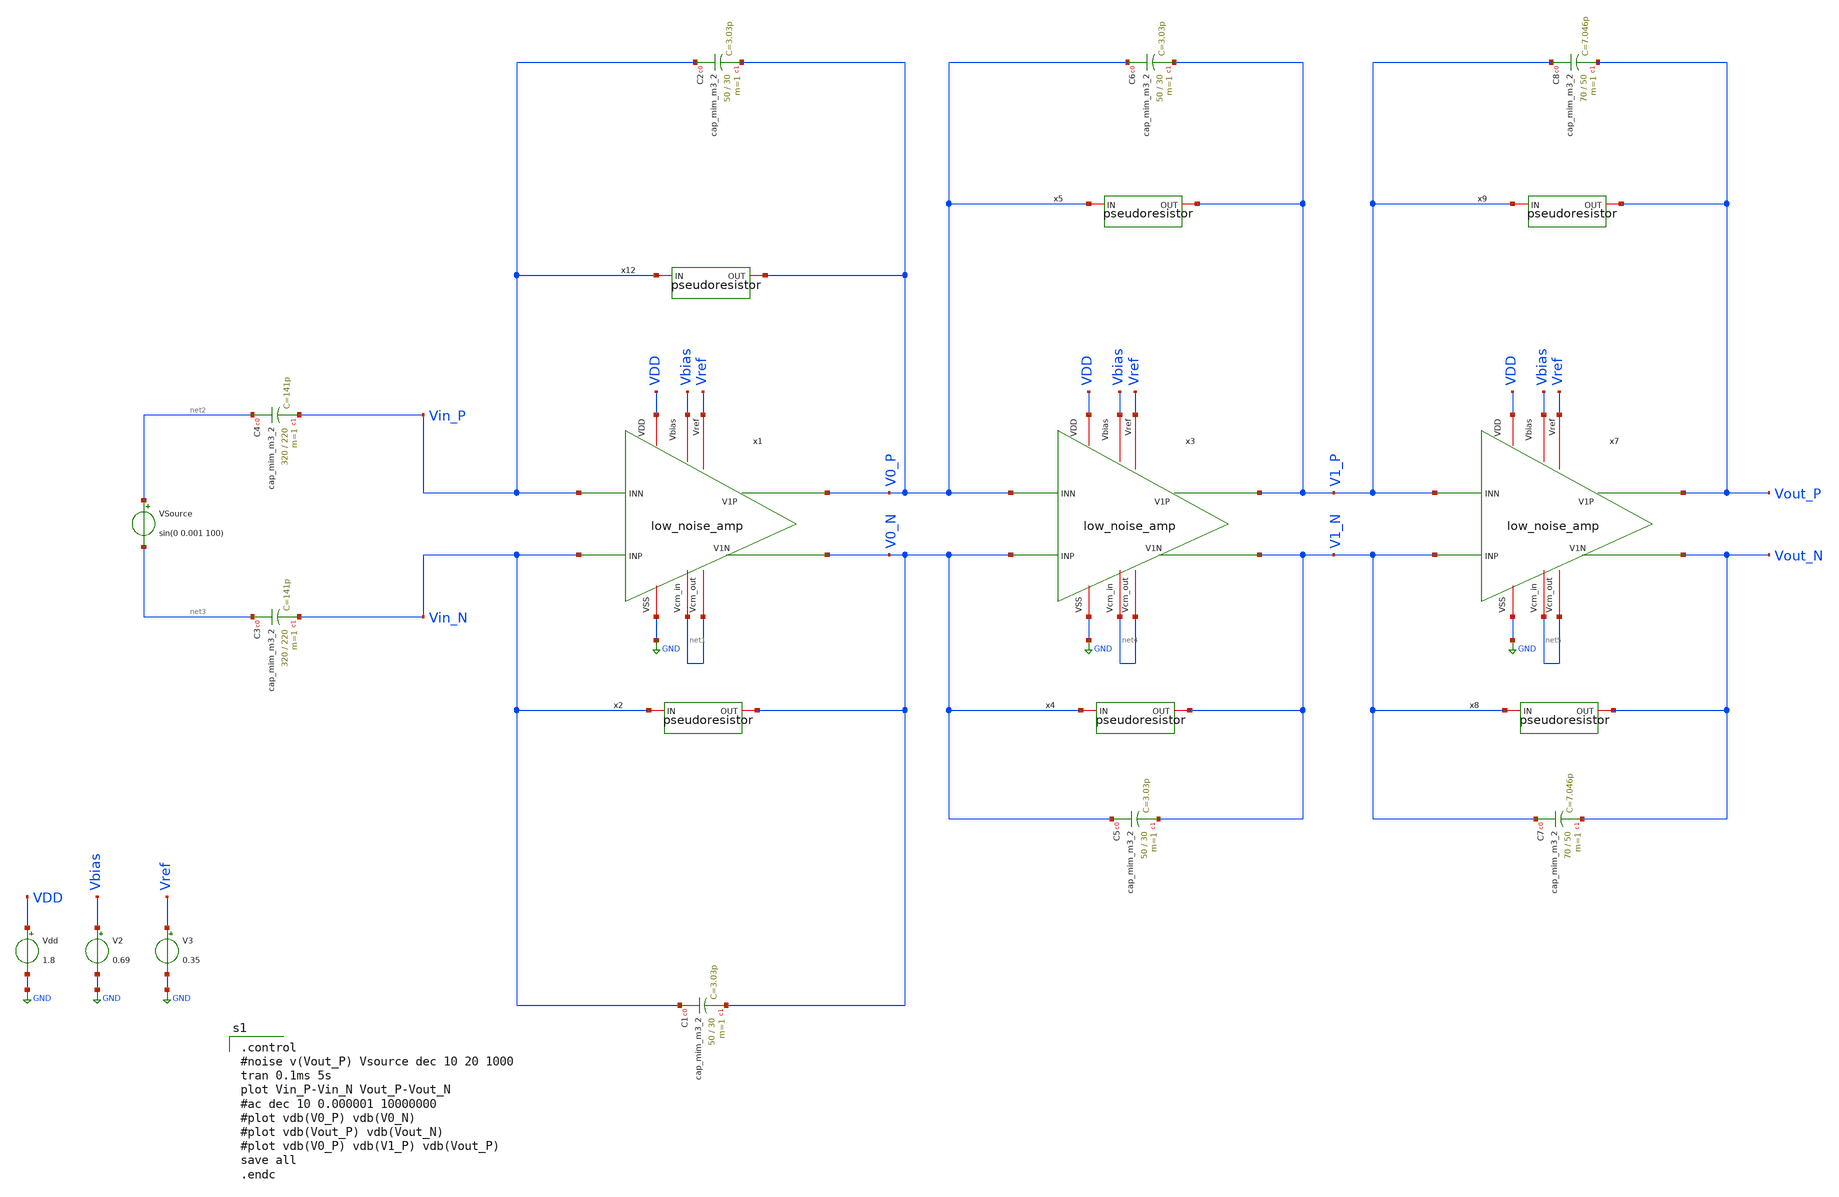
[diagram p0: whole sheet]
** sch_path: opamp_lna/low_noise_amp_tb.sch
**.subckt low_noise_amp_tb
x1 VDD net1 Vin_P Vin_N V0_P V0_N GND net1 Vbias Vref low_noise_amp
Vdd VDD GND 1.8
V2 Vbias GND 0.69
V3 Vref GND 0.35
VSource net2 net3 sin(0 0.001 100)
x2 Vin_N V0_N pseudoresistor
XC1 Vin_N V0_N sky130_fd_pr__cap_mim_m3_2 W=50 L=30 MF=1 m=1
XC2 Vin_P V0_P sky130_fd_pr__cap_mim_m3_2 W=50 L=30 MF=1 m=1
XC3 net3 Vin_N sky130_fd_pr__cap_mim_m3_2 W=320 L=220 MF=1 m=1
XC4 net2 Vin_P sky130_fd_pr__cap_mim_m3_2 W=320 L=220 MF=1 m=1
x3 VDD net4 V0_P V0_N V1_P V1_N GND net4 Vbias Vref low_noise_amp
x4 V0_N V1_N pseudoresistor
XC5 V0_N V1_N sky130_fd_pr__cap_mim_m3_2 W=50 L=30 MF=1 m=1
XC6 V0_P V1_P sky130_fd_pr__cap_mim_m3_2 W=50 L=30 MF=1 m=1
x5 V0_P V1_P pseudoresistor
x7 VDD net5 V1_P V1_N Vout_P Vout_N GND net5 Vbias Vref low_noise_amp
x8 V1_N Vout_N pseudoresistor
XC7 V1_N Vout_N sky130_fd_pr__cap_mim_m3_2 W=70 L=50 MF=1 m=1
XC8 V1_P Vout_P sky130_fd_pr__cap_mim_m3_2 W=70 L=50 MF=1 m=1
x9 V1_P Vout_P pseudoresistor
x12 Vin_P V0_P pseudoresistor
**** begin user architecture code

** opencircuitdesign pdks install
.lib $::SKYWATER_MODELS/sky130.lib.spice tt



.control
#noise v(Vout_P) Vsource dec 10 20 1000
tran 0.1ms 5s
plot Vin_P-Vin_N Vout_P-Vout_N
#ac dec 10 0.000001 10000000
#plot vdb(V0_P) vdb(V0_N)
#plot vdb(Vout_P) vdb(Vout_N)
#plot vdb(V0_P) vdb(V1_P) vdb(Vout_P)
save all
.endc

**** end user architecture code
**.ends

* expanding   symbol:  low_noise_amp.sym # of pins=10
** sym_path: opamp_lna/low_noise_amp.sym
** sch_path: opamp_lna/low_noise_amp.sch
.subckt low_noise_amp VDD Vcm_in INN INP V1P V1N VSS Vcm_out Vbias Vref
*.iopin VDD
*.iopin VSS
*.iopin Vbias
*.ipin INP
*.ipin INN
*.iopin Vref
*.iopin Vcm_in
*.iopin Vcm_out
*.opin V1N
*.opin V1P
XM3 CMFB Vref A0 VDD sky130_fd_pr__pfet_01v8 L=0.8 W=12 nf=1 ad='int((nf+1)/2) * W/nf * 0.29' as='int((nf+2)/2) * W/nf * 0.29'
+ pd='2*int((nf+1)/2) * (W/nf + 0.29)' ps='2*int((nf+2)/2) * (W/nf + 0.29)' nrd='0.29 / W' nrs='0.29 / W'
+ sa=0 sb=0 sd=0 mult=1 m=1
XM11 A0 Vbias VDD VDD sky130_fd_pr__pfet_01v8 L=0.8 W=4 nf=1 ad='int((nf+1)/2) * W/nf * 0.29' as='int((nf+2)/2) * W/nf * 0.29'
+ pd='2*int((nf+1)/2) * (W/nf + 0.29)' ps='2*int((nf+2)/2) * (W/nf + 0.29)' nrd='0.29 / W' nrs='0.29 / W'
+ sa=0 sb=0 sd=0 mult=1 m=1
XM7 V1N INP B0 VDD sky130_fd_pr__pfet_01v8 L=2 W=18 nf=1 ad='int((nf+1)/2) * W/nf * 0.29' as='int((nf+2)/2) * W/nf * 0.29'
+ pd='2*int((nf+1)/2) * (W/nf + 0.29)' ps='2*int((nf+2)/2) * (W/nf + 0.29)' nrd='0.29 / W' nrs='0.29 / W'
+ sa=0 sb=0 sd=0 mult=1 m=1
XM8 V1P INN B0 VDD sky130_fd_pr__pfet_01v8 L=2 W=18 nf=1 ad='int((nf+1)/2) * W/nf * 0.29' as='int((nf+2)/2) * W/nf * 0.29'
+ pd='2*int((nf+1)/2) * (W/nf + 0.29)' ps='2*int((nf+2)/2) * (W/nf + 0.29)' nrd='0.29 / W' nrs='0.29 / W'
+ sa=0 sb=0 sd=0 mult=1 m=1
XM9 V1N INP B1 VSS sky130_fd_pr__nfet_01v8 L=1 W=12 nf=1 ad='int((nf+1)/2) * W/nf * 0.29' as='int((nf+2)/2) * W/nf * 0.29'
+ pd='2*int((nf+1)/2) * (W/nf + 0.29)' ps='2*int((nf+2)/2) * (W/nf + 0.29)' nrd='0.29 / W' nrs='0.29 / W'
+ sa=0 sb=0 sd=0 mult=1 m=1
XM12 B0 Vbias VDD VDD sky130_fd_pr__pfet_01v8 L=0.8 W=4 nf=1 ad='int((nf+1)/2) * W/nf * 0.29' as='int((nf+2)/2) * W/nf * 0.29'
+ pd='2*int((nf+1)/2) * (W/nf + 0.29)' ps='2*int((nf+2)/2) * (W/nf + 0.29)' nrd='0.29 / W' nrs='0.29 / W'
+ sa=0 sb=0 sd=0 mult=1 m=1
XM13 B1 CMFB VSS VSS sky130_fd_pr__nfet_01v8 L=0.8 W=2 nf=1 ad='int((nf+1)/2) * W/nf * 0.29' as='int((nf+2)/2) * W/nf * 0.29'
+ pd='2*int((nf+1)/2) * (W/nf + 0.29)' ps='2*int((nf+2)/2) * (W/nf + 0.29)' nrd='0.29 / W' nrs='0.29 / W'
+ sa=0 sb=0 sd=0 mult=1 m=1
XM15 Vcm_out Vcm_out net1 Vcm_out sky130_fd_pr__pfet_01v8 L=0.6 W=1 nf=1 ad='int((nf+1)/2) * W/nf * 0.29'
+ as='int((nf+2)/2) * W/nf * 0.29' pd='2*int((nf+1)/2) * (W/nf + 0.29)' ps='2*int((nf+2)/2) * (W/nf + 0.29)'
+ nrd='0.29 / W' nrs='0.29 / W' sa=0 sb=0 sd=0 mult=5 m=5
XM16 net1 V1P V1P V1P sky130_fd_pr__pfet_01v8 L=0.6 W=1 nf=1 ad='int((nf+1)/2) * W/nf * 0.29' as='int((nf+2)/2) * W/nf * 0.29'
+ pd='2*int((nf+1)/2) * (W/nf + 0.29)' ps='2*int((nf+2)/2) * (W/nf + 0.29)' nrd='0.29 / W' nrs='0.29 / W'
+ sa=0 sb=0 sd=0 mult=5 m=5
XM17 Vcm_out Vcm_out net2 Vcm_out sky130_fd_pr__pfet_01v8 L=0.6 W=1 nf=1 ad='int((nf+1)/2) * W/nf * 0.29'
+ as='int((nf+2)/2) * W/nf * 0.29' pd='2*int((nf+1)/2) * (W/nf + 0.29)' ps='2*int((nf+2)/2) * (W/nf + 0.29)'
+ nrd='0.29 / W' nrs='0.29 / W' sa=0 sb=0 sd=0 mult=5 m=5
XM18 net2 V1N V1N V1N sky130_fd_pr__pfet_01v8 L=0.6 W=1 nf=1 ad='int((nf+1)/2) * W/nf * 0.29' as='int((nf+2)/2) * W/nf * 0.29'
+ pd='2*int((nf+1)/2) * (W/nf + 0.29)' ps='2*int((nf+2)/2) * (W/nf + 0.29)' nrd='0.29 / W' nrs='0.29 / W'
+ sa=0 sb=0 sd=0 mult=5 m=5
XC1 Vcm_out VSS sky130_fd_pr__cap_mim_m3_1 W=1 L=1 MF=1 m=1
XM1 V1P INN B1 VSS sky130_fd_pr__nfet_01v8 L=1 W=12 nf=1 ad='int((nf+1)/2) * W/nf * 0.29' as='int((nf+2)/2) * W/nf * 0.29'
+ pd='2*int((nf+1)/2) * (W/nf + 0.29)' ps='2*int((nf+2)/2) * (W/nf + 0.29)' nrd='0.29 / W' nrs='0.29 / W'
+ sa=0 sb=0 sd=0 mult=1 m=1
XM2 A1 A1 VSS VSS sky130_fd_pr__nfet_01v8 L=0.8 W=6 nf=1 ad='int((nf+1)/2) * W/nf * 0.29' as='int((nf+2)/2) * W/nf * 0.29'
+ pd='2*int((nf+1)/2) * (W/nf + 0.29)' ps='2*int((nf+2)/2) * (W/nf + 0.29)' nrd='0.29 / W' nrs='0.29 / W'
+ sa=0 sb=0 sd=0 mult=1 m=1
XM5 CMFB A1 VSS VSS sky130_fd_pr__nfet_01v8 L=0.8 W=6 nf=1 ad='int((nf+1)/2) * W/nf * 0.29' as='int((nf+2)/2) * W/nf * 0.29'
+ pd='2*int((nf+1)/2) * (W/nf + 0.29)' ps='2*int((nf+2)/2) * (W/nf + 0.29)' nrd='0.29 / W' nrs='0.29 / W'
+ sa=0 sb=0 sd=0 mult=1 m=1
XM6 A1 Vcm_in A0 VDD sky130_fd_pr__pfet_01v8 L=0.8 W=12 nf=1 ad='int((nf+1)/2) * W/nf * 0.29' as='int((nf+2)/2) * W/nf * 0.29'
+ pd='2*int((nf+1)/2) * (W/nf + 0.29)' ps='2*int((nf+2)/2) * (W/nf + 0.29)' nrd='0.29 / W' nrs='0.29 / W'
+ sa=0 sb=0 sd=0 mult=1 m=1
.ends


* expanding   symbol:  /home/lcg3895/CE393/pseudoresistor.sym # of pins=2
** sym_path: opamp_lna/pseudoresistor.sym
** sch_path: opamp_lna/pseudoresistor.sch
.subckt pseudoresistor IN OUT
*.iopin IN
*.iopin OUT
XM5 net1 IN IN IN sky130_fd_pr__pfet_01v8 L=0.5 W=1 nf=1 ad='int((nf+1)/2) * W/nf * 0.29' as='int((nf+2)/2) * W/nf * 0.29'
+ pd='2*int((nf+1)/2) * (W/nf + 0.29)' ps='2*int((nf+2)/2) * (W/nf + 0.29)' nrd='0.29 / W' nrs='0.29 / W'
+ sa=0 sb=0 sd=0 mult=10 m=10
XM1 net2 net2 net1 net2 sky130_fd_pr__pfet_01v8 L=0.5 W=1 nf=1 ad='int((nf+1)/2) * W/nf * 0.29' as='int((nf+2)/2) * W/nf * 0.29'
+ pd='2*int((nf+1)/2) * (W/nf + 0.29)' ps='2*int((nf+2)/2) * (W/nf + 0.29)' nrd='0.29 / W' nrs='0.29 / W'
+ sa=0 sb=0 sd=0 mult=10 m=10
XM2 net3 net2 net2 net2 sky130_fd_pr__pfet_01v8 L=0.5 W=1 nf=1 ad='int((nf+1)/2) * W/nf * 0.29' as='int((nf+2)/2) * W/nf * 0.29'
+ pd='2*int((nf+1)/2) * (W/nf + 0.29)' ps='2*int((nf+2)/2) * (W/nf + 0.29)' nrd='0.29 / W' nrs='0.29 / W'
+ sa=0 sb=0 sd=0 mult=10 m=10
XM3 OUT OUT net3 OUT sky130_fd_pr__pfet_01v8 L=0.5 W=1.2 nf=1 ad='int((nf+1)/2) * W/nf * 0.29' as='int((nf+2)/2) * W/nf * 0.29'
+ pd='2*int((nf+1)/2) * (W/nf + 0.29)' ps='2*int((nf+2)/2) * (W/nf + 0.29)' nrd='0.29 / W' nrs='0.29 / W'
+ sa=0 sb=0 sd=0 mult=1 m=1
.ends

.GLOBAL GND
.end
